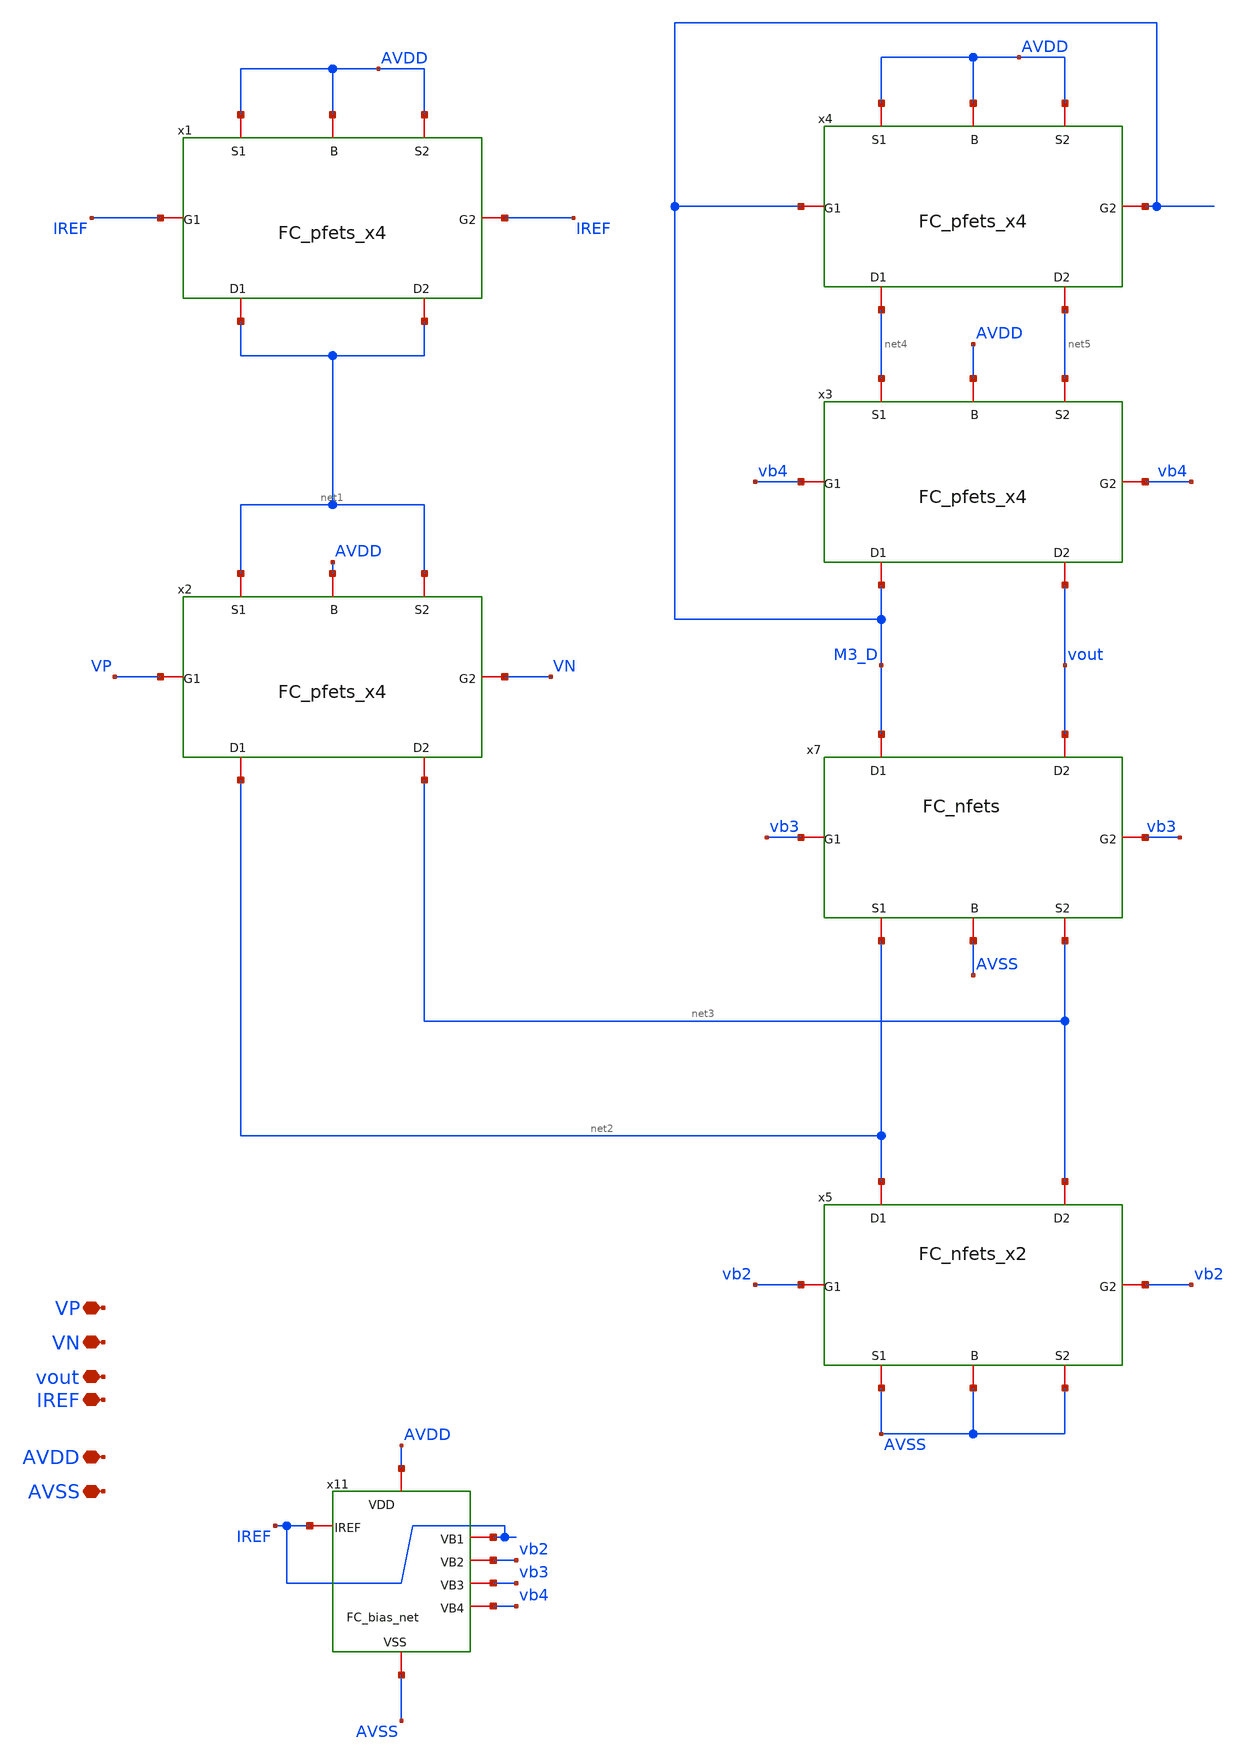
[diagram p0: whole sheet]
** sch_path: TIA_Filter/Folded/FoldedCascode.sch
**.subckt FoldedCascode AVDD AVSS vout VP VN IREF
*.iopin AVDD
*.iopin AVSS
*.iopin vout
*.iopin VP
*.iopin VN
*.iopin IREF
x7 net2 net3 M3_D vout vb3 vb3 AVSS FC_nfets
x5 AVSS AVSS net2 net3 vb2 vb2 AVSS FC_nfets_x2
x1 AVDD AVDD net1 net1 IREF IREF AVDD FC_pfets_x4
x2 net1 net1 net2 net3 VP VN AVDD FC_pfets_x4
x3 net4 net5 M3_D vout vb4 vb4 AVDD FC_pfets_x4
x4 AVDD AVDD net4 net5 M3_D M3_D AVDD FC_pfets_x4
x11 IREF IREF vb2 vb3 vb4 AVDD AVSS FC_bias_net
**.ends
.end
